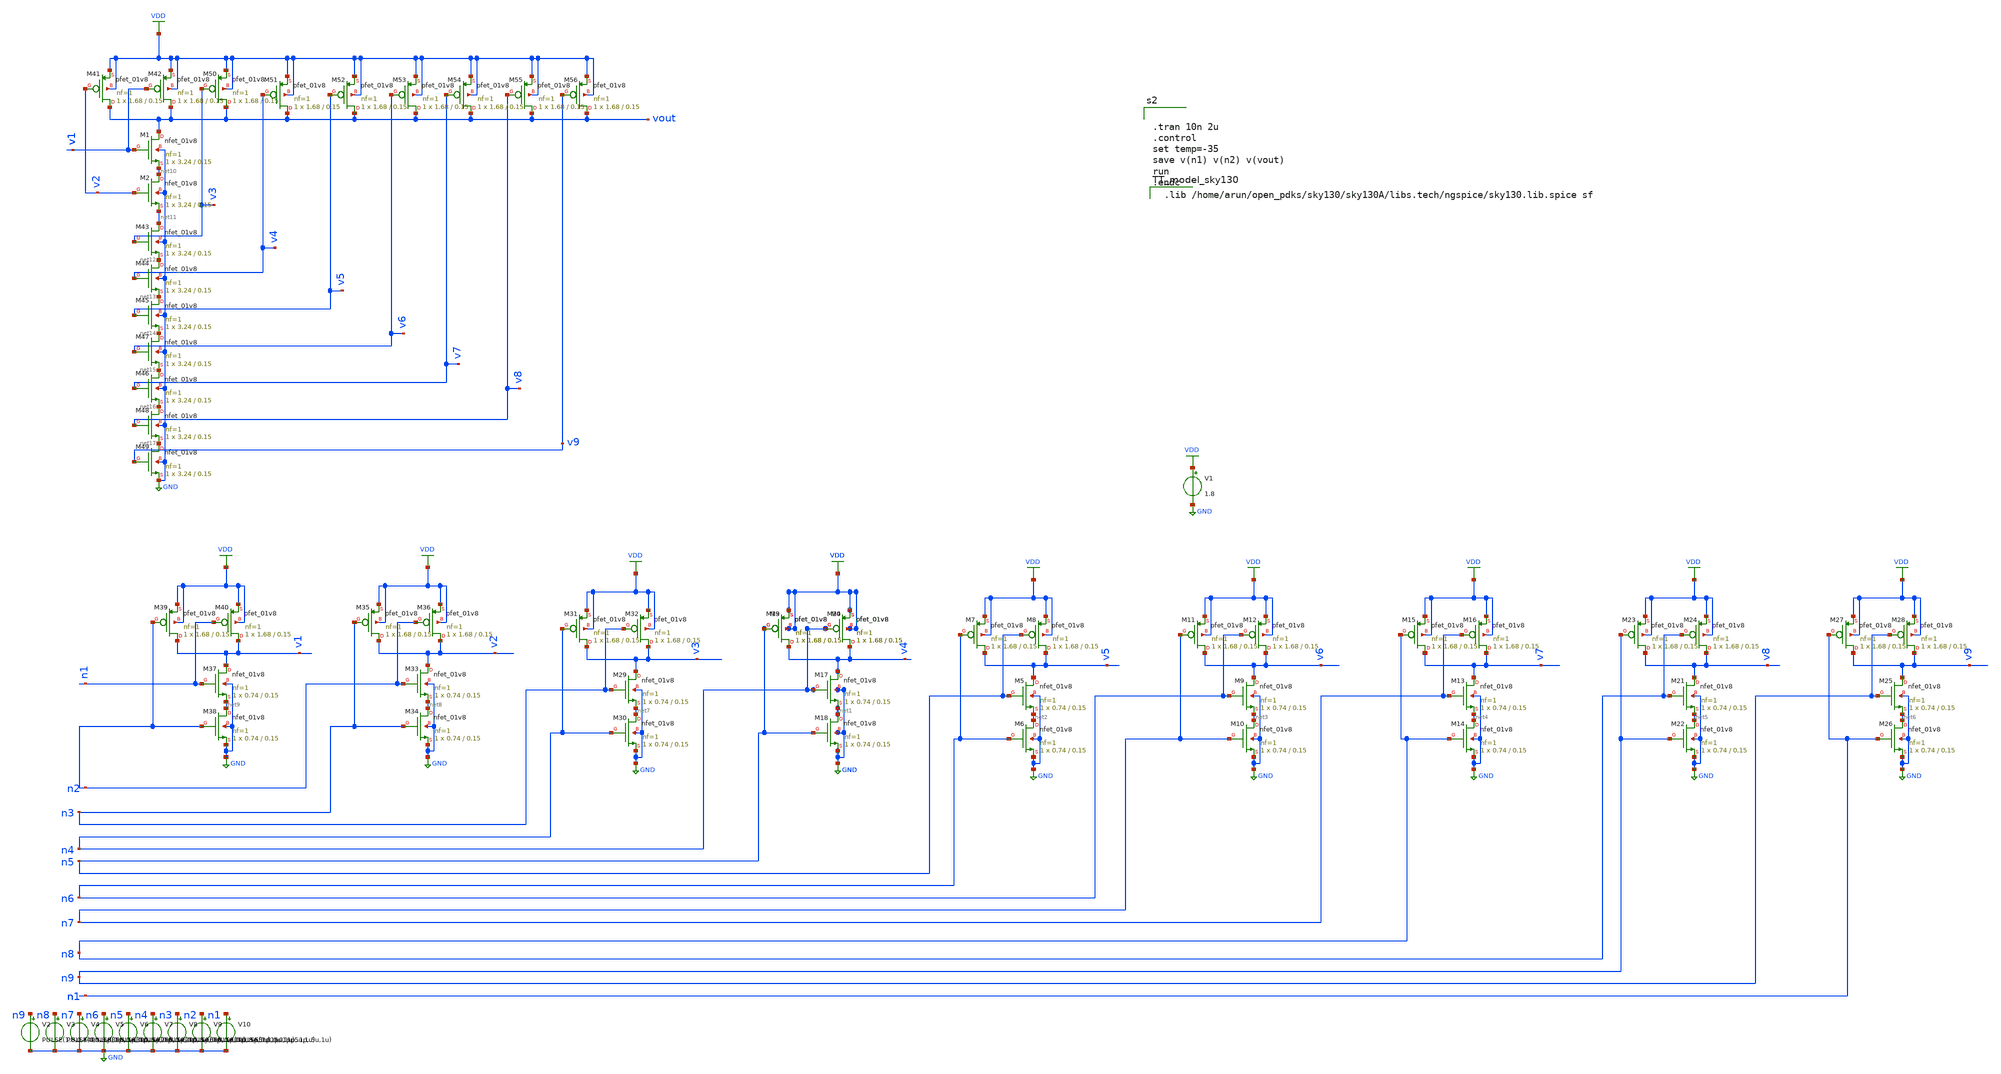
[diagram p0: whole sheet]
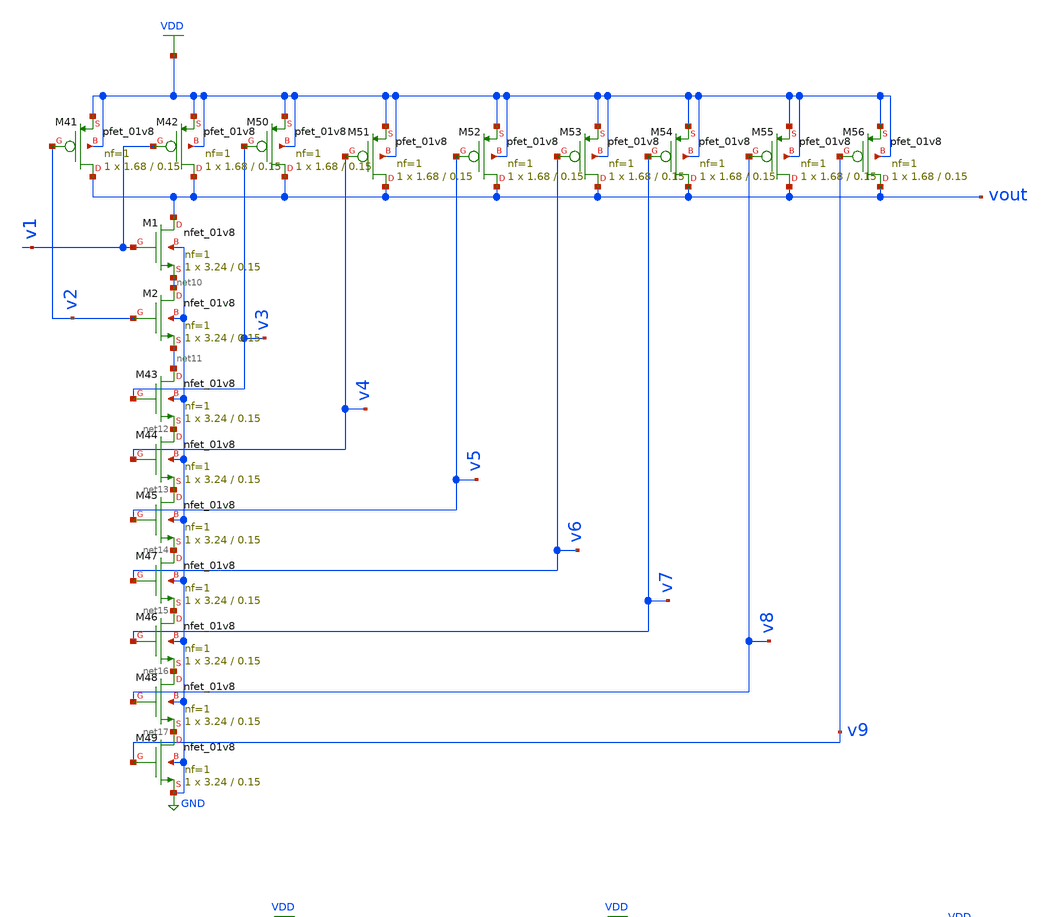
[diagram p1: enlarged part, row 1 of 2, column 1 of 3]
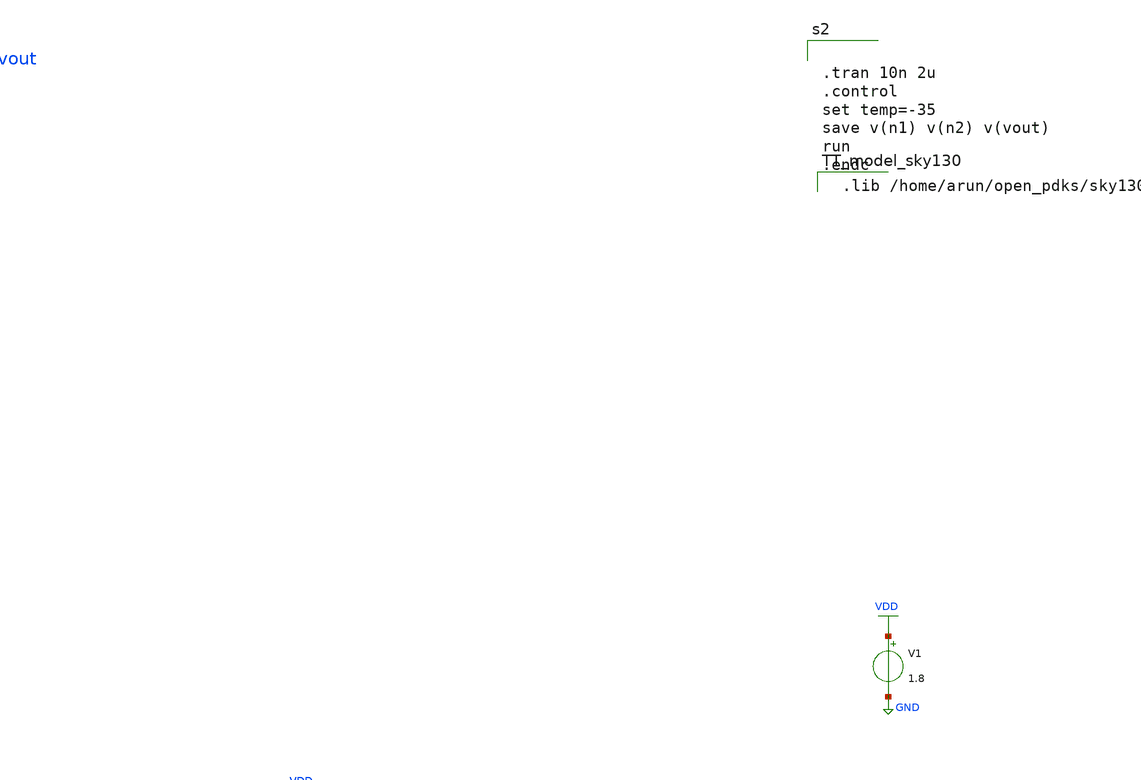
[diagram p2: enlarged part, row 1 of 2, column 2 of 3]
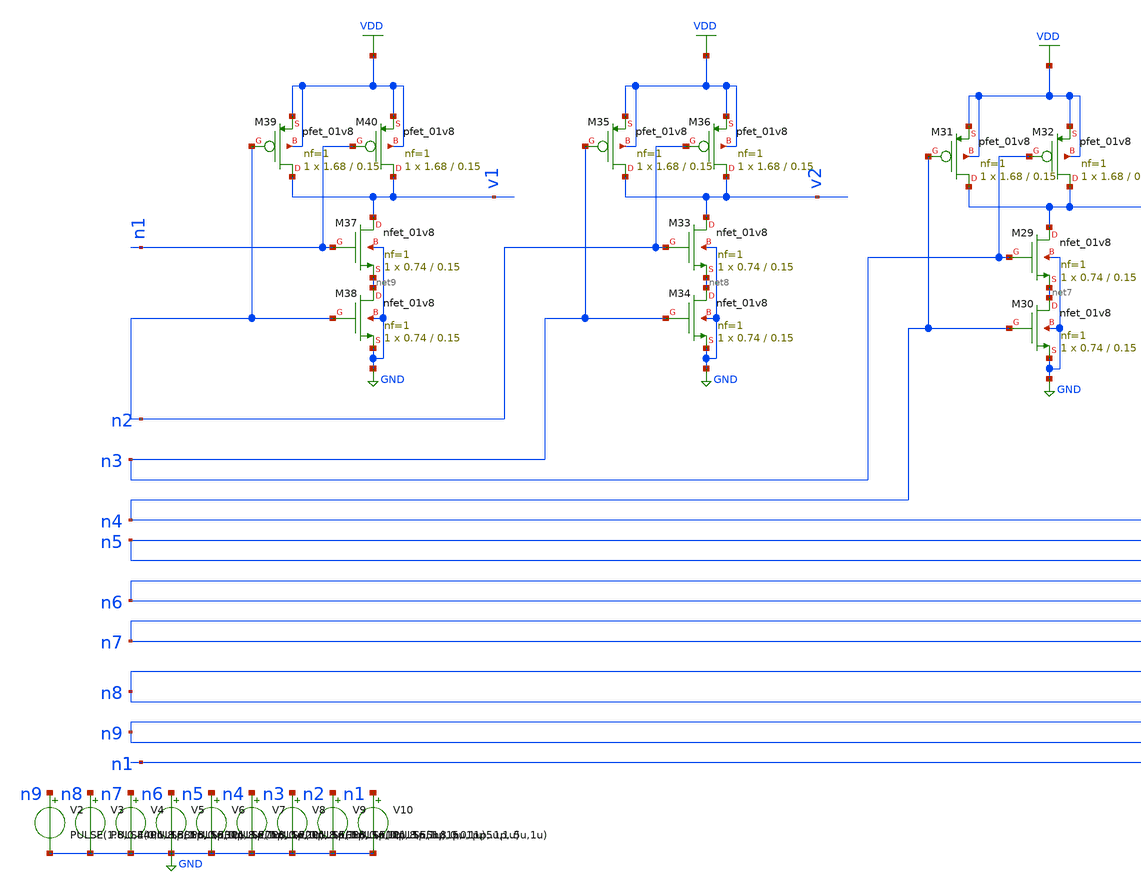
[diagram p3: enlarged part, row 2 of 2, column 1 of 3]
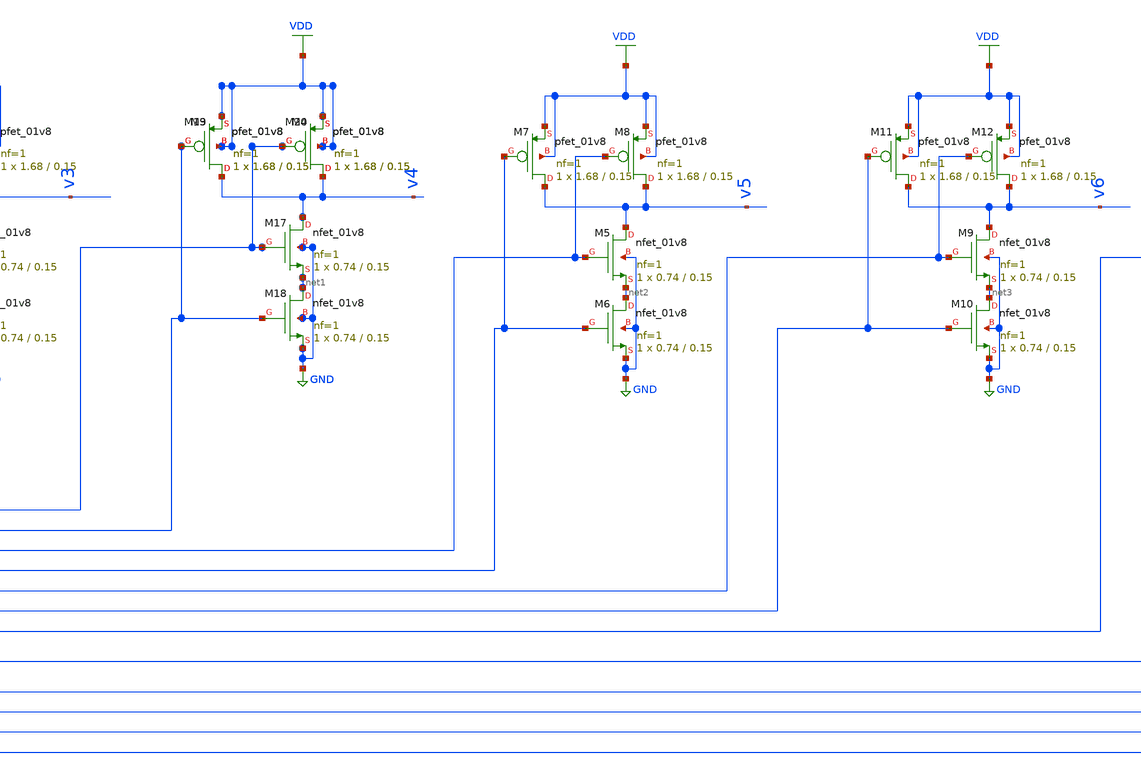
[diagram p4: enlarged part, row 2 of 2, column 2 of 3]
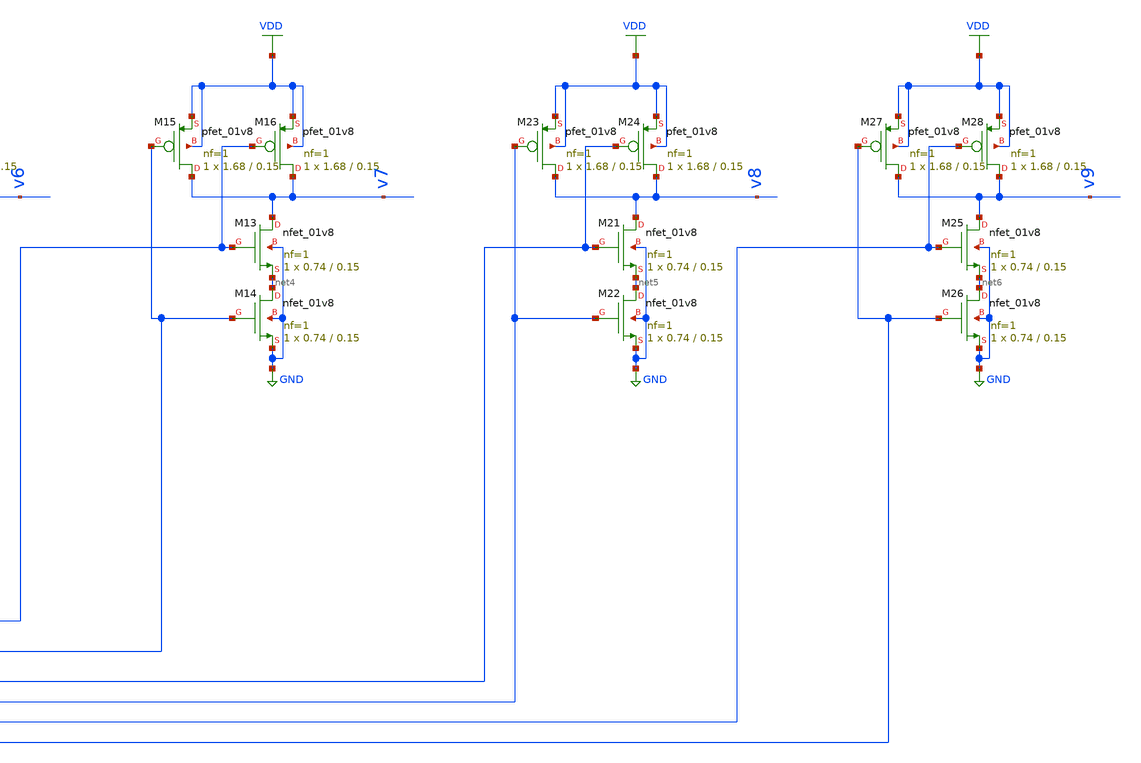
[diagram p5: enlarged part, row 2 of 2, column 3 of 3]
** sch_path: prelayout simulations/edge/edgecombiner.sch
**.subckt edgecombiner
XM3 v4 n5 VDD VDD sky130_fd_pr__pfet_01v8 L=0.15 W=1.68 nf=1 ad='int((nf+1)/2) * W/nf * 0.29' as='int((nf+2)/2) * W/nf * 0.29'
+ pd='2*int((nf+1)/2) * (W/nf + 0.29)' ps='2*int((nf+2)/2) * (W/nf + 0.29)' nrd='0.29 / W' nrs='0.29 / W'
+ sa=0 sb=0 sd=0 mult=1 m=1
XM4 v4 n4 VDD VDD sky130_fd_pr__pfet_01v8 L=0.15 W=1.68 nf=1 ad='int((nf+1)/2) * W/nf * 0.29' as='int((nf+2)/2) * W/nf * 0.29'
+ pd='2*int((nf+1)/2) * (W/nf + 0.29)' ps='2*int((nf+2)/2) * (W/nf + 0.29)' nrd='0.29 / W' nrs='0.29 / W'
+ sa=0 sb=0 sd=0 mult=1 m=1
XM5 v5 n5 net2 GND sky130_fd_pr__nfet_01v8 L=0.15 W=0.74 nf=1 ad='int((nf+1)/2) * W/nf * 0.29' as='int((nf+2)/2) * W/nf * 0.29'
+ pd='2*int((nf+1)/2) * (W/nf + 0.29)' ps='2*int((nf+2)/2) * (W/nf + 0.29)' nrd='0.29 / W' nrs='0.29 / W'
+ sa=0 sb=0 sd=0 mult=1 m=1
XM6 net2 n6 GND GND sky130_fd_pr__nfet_01v8 L=0.15 W=0.74 nf=1 ad='int((nf+1)/2) * W/nf * 0.29' as='int((nf+2)/2) * W/nf * 0.29'
+ pd='2*int((nf+1)/2) * (W/nf + 0.29)' ps='2*int((nf+2)/2) * (W/nf + 0.29)' nrd='0.29 / W' nrs='0.29 / W'
+ sa=0 sb=0 sd=0 mult=1 m=1
XM7 v5 n6 VDD VDD sky130_fd_pr__pfet_01v8 L=0.15 W=1.68 nf=1 ad='int((nf+1)/2) * W/nf * 0.29' as='int((nf+2)/2) * W/nf * 0.29'
+ pd='2*int((nf+1)/2) * (W/nf + 0.29)' ps='2*int((nf+2)/2) * (W/nf + 0.29)' nrd='0.29 / W' nrs='0.29 / W'
+ sa=0 sb=0 sd=0 mult=1 m=1
XM8 v5 n5 VDD VDD sky130_fd_pr__pfet_01v8 L=0.15 W=1.68 nf=1 ad='int((nf+1)/2) * W/nf * 0.29' as='int((nf+2)/2) * W/nf * 0.29'
+ pd='2*int((nf+1)/2) * (W/nf + 0.29)' ps='2*int((nf+2)/2) * (W/nf + 0.29)' nrd='0.29 / W' nrs='0.29 / W'
+ sa=0 sb=0 sd=0 mult=1 m=1
XM9 v6 n6 net3 GND sky130_fd_pr__nfet_01v8 L=0.15 W=0.74 nf=1 ad='int((nf+1)/2) * W/nf * 0.29' as='int((nf+2)/2) * W/nf * 0.29'
+ pd='2*int((nf+1)/2) * (W/nf + 0.29)' ps='2*int((nf+2)/2) * (W/nf + 0.29)' nrd='0.29 / W' nrs='0.29 / W'
+ sa=0 sb=0 sd=0 mult=1 m=1
XM10 net3 n7 GND GND sky130_fd_pr__nfet_01v8 L=0.15 W=0.74 nf=1 ad='int((nf+1)/2) * W/nf * 0.29' as='int((nf+2)/2) * W/nf * 0.29'
+ pd='2*int((nf+1)/2) * (W/nf + 0.29)' ps='2*int((nf+2)/2) * (W/nf + 0.29)' nrd='0.29 / W' nrs='0.29 / W'
+ sa=0 sb=0 sd=0 mult=1 m=1
XM11 v6 n7 VDD VDD sky130_fd_pr__pfet_01v8 L=0.15 W=1.68 nf=1 ad='int((nf+1)/2) * W/nf * 0.29' as='int((nf+2)/2) * W/nf * 0.29'
+ pd='2*int((nf+1)/2) * (W/nf + 0.29)' ps='2*int((nf+2)/2) * (W/nf + 0.29)' nrd='0.29 / W' nrs='0.29 / W'
+ sa=0 sb=0 sd=0 mult=1 m=1
XM12 v6 n6 VDD VDD sky130_fd_pr__pfet_01v8 L=0.15 W=1.68 nf=1 ad='int((nf+1)/2) * W/nf * 0.29' as='int((nf+2)/2) * W/nf * 0.29'
+ pd='2*int((nf+1)/2) * (W/nf + 0.29)' ps='2*int((nf+2)/2) * (W/nf + 0.29)' nrd='0.29 / W' nrs='0.29 / W'
+ sa=0 sb=0 sd=0 mult=1 m=1
XM13 v7 n7 net4 GND sky130_fd_pr__nfet_01v8 L=0.15 W=0.74 nf=1 ad='int((nf+1)/2) * W/nf * 0.29' as='int((nf+2)/2) * W/nf * 0.29'
+ pd='2*int((nf+1)/2) * (W/nf + 0.29)' ps='2*int((nf+2)/2) * (W/nf + 0.29)' nrd='0.29 / W' nrs='0.29 / W'
+ sa=0 sb=0 sd=0 mult=1 m=1
XM14 net4 n8 GND GND sky130_fd_pr__nfet_01v8 L=0.15 W=0.74 nf=1 ad='int((nf+1)/2) * W/nf * 0.29' as='int((nf+2)/2) * W/nf * 0.29'
+ pd='2*int((nf+1)/2) * (W/nf + 0.29)' ps='2*int((nf+2)/2) * (W/nf + 0.29)' nrd='0.29 / W' nrs='0.29 / W'
+ sa=0 sb=0 sd=0 mult=1 m=1
XM15 v7 n8 VDD VDD sky130_fd_pr__pfet_01v8 L=0.15 W=1.68 nf=1 ad='int((nf+1)/2) * W/nf * 0.29' as='int((nf+2)/2) * W/nf * 0.29'
+ pd='2*int((nf+1)/2) * (W/nf + 0.29)' ps='2*int((nf+2)/2) * (W/nf + 0.29)' nrd='0.29 / W' nrs='0.29 / W'
+ sa=0 sb=0 sd=0 mult=1 m=1
XM16 v7 n7 VDD VDD sky130_fd_pr__pfet_01v8 L=0.15 W=1.68 nf=1 ad='int((nf+1)/2) * W/nf * 0.29' as='int((nf+2)/2) * W/nf * 0.29'
+ pd='2*int((nf+1)/2) * (W/nf + 0.29)' ps='2*int((nf+2)/2) * (W/nf + 0.29)' nrd='0.29 / W' nrs='0.29 / W'
+ sa=0 sb=0 sd=0 mult=1 m=1
XM17 v4 n4 net1 GND sky130_fd_pr__nfet_01v8 L=0.15 W=0.74 nf=1 ad='int((nf+1)/2) * W/nf * 0.29' as='int((nf+2)/2) * W/nf * 0.29'
+ pd='2*int((nf+1)/2) * (W/nf + 0.29)' ps='2*int((nf+2)/2) * (W/nf + 0.29)' nrd='0.29 / W' nrs='0.29 / W'
+ sa=0 sb=0 sd=0 mult=1 m=1
XM18 net1 n5 GND GND sky130_fd_pr__nfet_01v8 L=0.15 W=0.74 nf=1 ad='int((nf+1)/2) * W/nf * 0.29' as='int((nf+2)/2) * W/nf * 0.29'
+ pd='2*int((nf+1)/2) * (W/nf + 0.29)' ps='2*int((nf+2)/2) * (W/nf + 0.29)' nrd='0.29 / W' nrs='0.29 / W'
+ sa=0 sb=0 sd=0 mult=1 m=1
XM19 v4 n5 VDD VDD sky130_fd_pr__pfet_01v8 L=0.15 W=1.68 nf=1 ad='int((nf+1)/2) * W/nf * 0.29' as='int((nf+2)/2) * W/nf * 0.29'
+ pd='2*int((nf+1)/2) * (W/nf + 0.29)' ps='2*int((nf+2)/2) * (W/nf + 0.29)' nrd='0.29 / W' nrs='0.29 / W'
+ sa=0 sb=0 sd=0 mult=1 m=1
XM20 v4 n4 VDD VDD sky130_fd_pr__pfet_01v8 L=0.15 W=1.68 nf=1 ad='int((nf+1)/2) * W/nf * 0.29' as='int((nf+2)/2) * W/nf * 0.29'
+ pd='2*int((nf+1)/2) * (W/nf + 0.29)' ps='2*int((nf+2)/2) * (W/nf + 0.29)' nrd='0.29 / W' nrs='0.29 / W'
+ sa=0 sb=0 sd=0 mult=1 m=1
XM21 v8 n8 net5 GND sky130_fd_pr__nfet_01v8 L=0.15 W=0.74 nf=1 ad='int((nf+1)/2) * W/nf * 0.29' as='int((nf+2)/2) * W/nf * 0.29'
+ pd='2*int((nf+1)/2) * (W/nf + 0.29)' ps='2*int((nf+2)/2) * (W/nf + 0.29)' nrd='0.29 / W' nrs='0.29 / W'
+ sa=0 sb=0 sd=0 mult=1 m=1
XM22 net5 n9 GND GND sky130_fd_pr__nfet_01v8 L=0.15 W=0.74 nf=1 ad='int((nf+1)/2) * W/nf * 0.29' as='int((nf+2)/2) * W/nf * 0.29'
+ pd='2*int((nf+1)/2) * (W/nf + 0.29)' ps='2*int((nf+2)/2) * (W/nf + 0.29)' nrd='0.29 / W' nrs='0.29 / W'
+ sa=0 sb=0 sd=0 mult=1 m=1
XM23 v8 n9 VDD VDD sky130_fd_pr__pfet_01v8 L=0.15 W=1.68 nf=1 ad='int((nf+1)/2) * W/nf * 0.29' as='int((nf+2)/2) * W/nf * 0.29'
+ pd='2*int((nf+1)/2) * (W/nf + 0.29)' ps='2*int((nf+2)/2) * (W/nf + 0.29)' nrd='0.29 / W' nrs='0.29 / W'
+ sa=0 sb=0 sd=0 mult=1 m=1
XM24 v8 n8 VDD VDD sky130_fd_pr__pfet_01v8 L=0.15 W=1.68 nf=1 ad='int((nf+1)/2) * W/nf * 0.29' as='int((nf+2)/2) * W/nf * 0.29'
+ pd='2*int((nf+1)/2) * (W/nf + 0.29)' ps='2*int((nf+2)/2) * (W/nf + 0.29)' nrd='0.29 / W' nrs='0.29 / W'
+ sa=0 sb=0 sd=0 mult=1 m=1
XM25 v9 n9 net6 GND sky130_fd_pr__nfet_01v8 L=0.15 W=0.74 nf=1 ad='int((nf+1)/2) * W/nf * 0.29' as='int((nf+2)/2) * W/nf * 0.29'
+ pd='2*int((nf+1)/2) * (W/nf + 0.29)' ps='2*int((nf+2)/2) * (W/nf + 0.29)' nrd='0.29 / W' nrs='0.29 / W'
+ sa=0 sb=0 sd=0 mult=1 m=1
XM26 net6 n1 GND GND sky130_fd_pr__nfet_01v8 L=0.15 W=0.74 nf=1 ad='int((nf+1)/2) * W/nf * 0.29' as='int((nf+2)/2) * W/nf * 0.29'
+ pd='2*int((nf+1)/2) * (W/nf + 0.29)' ps='2*int((nf+2)/2) * (W/nf + 0.29)' nrd='0.29 / W' nrs='0.29 / W'
+ sa=0 sb=0 sd=0 mult=1 m=1
XM27 v9 n1 VDD VDD sky130_fd_pr__pfet_01v8 L=0.15 W=1.68 nf=1 ad='int((nf+1)/2) * W/nf * 0.29' as='int((nf+2)/2) * W/nf * 0.29'
+ pd='2*int((nf+1)/2) * (W/nf + 0.29)' ps='2*int((nf+2)/2) * (W/nf + 0.29)' nrd='0.29 / W' nrs='0.29 / W'
+ sa=0 sb=0 sd=0 mult=1 m=1
XM28 v9 n9 VDD VDD sky130_fd_pr__pfet_01v8 L=0.15 W=1.68 nf=1 ad='int((nf+1)/2) * W/nf * 0.29' as='int((nf+2)/2) * W/nf * 0.29'
+ pd='2*int((nf+1)/2) * (W/nf + 0.29)' ps='2*int((nf+2)/2) * (W/nf + 0.29)' nrd='0.29 / W' nrs='0.29 / W'
+ sa=0 sb=0 sd=0 mult=1 m=1
XM29 v3 n3 net7 GND sky130_fd_pr__nfet_01v8 L=0.15 W=0.74 nf=1 ad='int((nf+1)/2) * W/nf * 0.29' as='int((nf+2)/2) * W/nf * 0.29'
+ pd='2*int((nf+1)/2) * (W/nf + 0.29)' ps='2*int((nf+2)/2) * (W/nf + 0.29)' nrd='0.29 / W' nrs='0.29 / W'
+ sa=0 sb=0 sd=0 mult=1 m=1
XM30 net7 n4 GND GND sky130_fd_pr__nfet_01v8 L=0.15 W=0.74 nf=1 ad='int((nf+1)/2) * W/nf * 0.29' as='int((nf+2)/2) * W/nf * 0.29'
+ pd='2*int((nf+1)/2) * (W/nf + 0.29)' ps='2*int((nf+2)/2) * (W/nf + 0.29)' nrd='0.29 / W' nrs='0.29 / W'
+ sa=0 sb=0 sd=0 mult=1 m=1
XM31 v3 n4 VDD VDD sky130_fd_pr__pfet_01v8 L=0.15 W=1.68 nf=1 ad='int((nf+1)/2) * W/nf * 0.29' as='int((nf+2)/2) * W/nf * 0.29'
+ pd='2*int((nf+1)/2) * (W/nf + 0.29)' ps='2*int((nf+2)/2) * (W/nf + 0.29)' nrd='0.29 / W' nrs='0.29 / W'
+ sa=0 sb=0 sd=0 mult=1 m=1
XM32 v3 n3 VDD VDD sky130_fd_pr__pfet_01v8 L=0.15 W=1.68 nf=1 ad='int((nf+1)/2) * W/nf * 0.29' as='int((nf+2)/2) * W/nf * 0.29'
+ pd='2*int((nf+1)/2) * (W/nf + 0.29)' ps='2*int((nf+2)/2) * (W/nf + 0.29)' nrd='0.29 / W' nrs='0.29 / W'
+ sa=0 sb=0 sd=0 mult=1 m=1
XM33 v2 n2 net8 GND sky130_fd_pr__nfet_01v8 L=0.15 W=0.74 nf=1 ad='int((nf+1)/2) * W/nf * 0.29' as='int((nf+2)/2) * W/nf * 0.29'
+ pd='2*int((nf+1)/2) * (W/nf + 0.29)' ps='2*int((nf+2)/2) * (W/nf + 0.29)' nrd='0.29 / W' nrs='0.29 / W'
+ sa=0 sb=0 sd=0 mult=1 m=1
XM34 net8 n3 GND GND sky130_fd_pr__nfet_01v8 L=0.15 W=0.74 nf=1 ad='int((nf+1)/2) * W/nf * 0.29' as='int((nf+2)/2) * W/nf * 0.29'
+ pd='2*int((nf+1)/2) * (W/nf + 0.29)' ps='2*int((nf+2)/2) * (W/nf + 0.29)' nrd='0.29 / W' nrs='0.29 / W'
+ sa=0 sb=0 sd=0 mult=1 m=1
XM35 v2 n3 VDD VDD sky130_fd_pr__pfet_01v8 L=0.15 W=1.68 nf=1 ad='int((nf+1)/2) * W/nf * 0.29' as='int((nf+2)/2) * W/nf * 0.29'
+ pd='2*int((nf+1)/2) * (W/nf + 0.29)' ps='2*int((nf+2)/2) * (W/nf + 0.29)' nrd='0.29 / W' nrs='0.29 / W'
+ sa=0 sb=0 sd=0 mult=1 m=1
XM36 v2 n2 VDD VDD sky130_fd_pr__pfet_01v8 L=0.15 W=1.68 nf=1 ad='int((nf+1)/2) * W/nf * 0.29' as='int((nf+2)/2) * W/nf * 0.29'
+ pd='2*int((nf+1)/2) * (W/nf + 0.29)' ps='2*int((nf+2)/2) * (W/nf + 0.29)' nrd='0.29 / W' nrs='0.29 / W'
+ sa=0 sb=0 sd=0 mult=1 m=1
XM37 v1 n1 net9 GND sky130_fd_pr__nfet_01v8 L=0.15 W=0.74 nf=1 ad='int((nf+1)/2) * W/nf * 0.29' as='int((nf+2)/2) * W/nf * 0.29'
+ pd='2*int((nf+1)/2) * (W/nf + 0.29)' ps='2*int((nf+2)/2) * (W/nf + 0.29)' nrd='0.29 / W' nrs='0.29 / W'
+ sa=0 sb=0 sd=0 mult=1 m=1
XM38 net9 n2 GND GND sky130_fd_pr__nfet_01v8 L=0.15 W=0.74 nf=1 ad='int((nf+1)/2) * W/nf * 0.29' as='int((nf+2)/2) * W/nf * 0.29'
+ pd='2*int((nf+1)/2) * (W/nf + 0.29)' ps='2*int((nf+2)/2) * (W/nf + 0.29)' nrd='0.29 / W' nrs='0.29 / W'
+ sa=0 sb=0 sd=0 mult=1 m=1
XM39 v1 n2 VDD VDD sky130_fd_pr__pfet_01v8 L=0.15 W=1.68 nf=1 ad='int((nf+1)/2) * W/nf * 0.29' as='int((nf+2)/2) * W/nf * 0.29'
+ pd='2*int((nf+1)/2) * (W/nf + 0.29)' ps='2*int((nf+2)/2) * (W/nf + 0.29)' nrd='0.29 / W' nrs='0.29 / W'
+ sa=0 sb=0 sd=0 mult=1 m=1
XM40 v1 n1 VDD VDD sky130_fd_pr__pfet_01v8 L=0.15 W=1.68 nf=1 ad='int((nf+1)/2) * W/nf * 0.29' as='int((nf+2)/2) * W/nf * 0.29'
+ pd='2*int((nf+1)/2) * (W/nf + 0.29)' ps='2*int((nf+2)/2) * (W/nf + 0.29)' nrd='0.29 / W' nrs='0.29 / W'
+ sa=0 sb=0 sd=0 mult=1 m=1
V1 VDD GND 1.8
XM1 vout v1 net10 GND sky130_fd_pr__nfet_01v8 L=0.15 W=3.24 nf=1 ad='int((nf+1)/2) * W/nf * 0.29' as='int((nf+2)/2) * W/nf * 0.29'
+ pd='2*int((nf+1)/2) * (W/nf + 0.29)' ps='2*int((nf+2)/2) * (W/nf + 0.29)' nrd='0.29 / W' nrs='0.29 / W'
+ sa=0 sb=0 sd=0 mult=1 m=1
XM2 net10 v2 net11 GND sky130_fd_pr__nfet_01v8 L=0.15 W=3.24 nf=1 ad='int((nf+1)/2) * W/nf * 0.29' as='int((nf+2)/2) * W/nf * 0.29'
+ pd='2*int((nf+1)/2) * (W/nf + 0.29)' ps='2*int((nf+2)/2) * (W/nf + 0.29)' nrd='0.29 / W' nrs='0.29 / W'
+ sa=0 sb=0 sd=0 mult=1 m=1
XM41 vout v2 VDD VDD sky130_fd_pr__pfet_01v8 L=0.15 W=1.68 nf=1 ad='int((nf+1)/2) * W/nf * 0.29' as='int((nf+2)/2) * W/nf * 0.29'
+ pd='2*int((nf+1)/2) * (W/nf + 0.29)' ps='2*int((nf+2)/2) * (W/nf + 0.29)' nrd='0.29 / W' nrs='0.29 / W'
+ sa=0 sb=0 sd=0 mult=1 m=1
XM42 vout v1 VDD VDD sky130_fd_pr__pfet_01v8 L=0.15 W=1.68 nf=1 ad='int((nf+1)/2) * W/nf * 0.29' as='int((nf+2)/2) * W/nf * 0.29'
+ pd='2*int((nf+1)/2) * (W/nf + 0.29)' ps='2*int((nf+2)/2) * (W/nf + 0.29)' nrd='0.29 / W' nrs='0.29 / W'
+ sa=0 sb=0 sd=0 mult=1 m=1
XM43 net11 v3 net12 GND sky130_fd_pr__nfet_01v8 L=0.15 W=3.24 nf=1 ad='int((nf+1)/2) * W/nf * 0.29' as='int((nf+2)/2) * W/nf * 0.29'
+ pd='2*int((nf+1)/2) * (W/nf + 0.29)' ps='2*int((nf+2)/2) * (W/nf + 0.29)' nrd='0.29 / W' nrs='0.29 / W'
+ sa=0 sb=0 sd=0 mult=1 m=1
XM44 net12 v4 net13 GND sky130_fd_pr__nfet_01v8 L=0.15 W=3.24 nf=1 ad='int((nf+1)/2) * W/nf * 0.29' as='int((nf+2)/2) * W/nf * 0.29'
+ pd='2*int((nf+1)/2) * (W/nf + 0.29)' ps='2*int((nf+2)/2) * (W/nf + 0.29)' nrd='0.29 / W' nrs='0.29 / W'
+ sa=0 sb=0 sd=0 mult=1 m=1
XM45 net13 v5 net14 GND sky130_fd_pr__nfet_01v8 L=0.15 W=3.24 nf=1 ad='int((nf+1)/2) * W/nf * 0.29' as='int((nf+2)/2) * W/nf * 0.29'
+ pd='2*int((nf+1)/2) * (W/nf + 0.29)' ps='2*int((nf+2)/2) * (W/nf + 0.29)' nrd='0.29 / W' nrs='0.29 / W'
+ sa=0 sb=0 sd=0 mult=1 m=1
XM46 net15 v7 net16 GND sky130_fd_pr__nfet_01v8 L=0.15 W=3.24 nf=1 ad='int((nf+1)/2) * W/nf * 0.29' as='int((nf+2)/2) * W/nf * 0.29'
+ pd='2*int((nf+1)/2) * (W/nf + 0.29)' ps='2*int((nf+2)/2) * (W/nf + 0.29)' nrd='0.29 / W' nrs='0.29 / W'
+ sa=0 sb=0 sd=0 mult=1 m=1
XM47 net14 v6 net15 GND sky130_fd_pr__nfet_01v8 L=0.15 W=3.24 nf=1 ad='int((nf+1)/2) * W/nf * 0.29' as='int((nf+2)/2) * W/nf * 0.29'
+ pd='2*int((nf+1)/2) * (W/nf + 0.29)' ps='2*int((nf+2)/2) * (W/nf + 0.29)' nrd='0.29 / W' nrs='0.29 / W'
+ sa=0 sb=0 sd=0 mult=1 m=1
XM48 net16 v8 net17 GND sky130_fd_pr__nfet_01v8 L=0.15 W=3.24 nf=1 ad='int((nf+1)/2) * W/nf * 0.29' as='int((nf+2)/2) * W/nf * 0.29'
+ pd='2*int((nf+1)/2) * (W/nf + 0.29)' ps='2*int((nf+2)/2) * (W/nf + 0.29)' nrd='0.29 / W' nrs='0.29 / W'
+ sa=0 sb=0 sd=0 mult=1 m=1
XM49 net17 v9 GND GND sky130_fd_pr__nfet_01v8 L=0.15 W=3.24 nf=1 ad='int((nf+1)/2) * W/nf * 0.29' as='int((nf+2)/2) * W/nf * 0.29'
+ pd='2*int((nf+1)/2) * (W/nf + 0.29)' ps='2*int((nf+2)/2) * (W/nf + 0.29)' nrd='0.29 / W' nrs='0.29 / W'
+ sa=0 sb=0 sd=0 mult=1 m=1
XM51 vout v4 VDD VDD sky130_fd_pr__pfet_01v8 L=0.15 W=1.68 nf=1 ad='int((nf+1)/2) * W/nf * 0.29' as='int((nf+2)/2) * W/nf * 0.29'
+ pd='2*int((nf+1)/2) * (W/nf + 0.29)' ps='2*int((nf+2)/2) * (W/nf + 0.29)' nrd='0.29 / W' nrs='0.29 / W'
+ sa=0 sb=0 sd=0 mult=1 m=1
XM52 vout v5 VDD VDD sky130_fd_pr__pfet_01v8 L=0.15 W=1.68 nf=1 ad='int((nf+1)/2) * W/nf * 0.29' as='int((nf+2)/2) * W/nf * 0.29'
+ pd='2*int((nf+1)/2) * (W/nf + 0.29)' ps='2*int((nf+2)/2) * (W/nf + 0.29)' nrd='0.29 / W' nrs='0.29 / W'
+ sa=0 sb=0 sd=0 mult=1 m=1
XM53 vout v6 VDD VDD sky130_fd_pr__pfet_01v8 L=0.15 W=1.68 nf=1 ad='int((nf+1)/2) * W/nf * 0.29' as='int((nf+2)/2) * W/nf * 0.29'
+ pd='2*int((nf+1)/2) * (W/nf + 0.29)' ps='2*int((nf+2)/2) * (W/nf + 0.29)' nrd='0.29 / W' nrs='0.29 / W'
+ sa=0 sb=0 sd=0 mult=1 m=1
XM54 vout v7 VDD VDD sky130_fd_pr__pfet_01v8 L=0.15 W=1.68 nf=1 ad='int((nf+1)/2) * W/nf * 0.29' as='int((nf+2)/2) * W/nf * 0.29'
+ pd='2*int((nf+1)/2) * (W/nf + 0.29)' ps='2*int((nf+2)/2) * (W/nf + 0.29)' nrd='0.29 / W' nrs='0.29 / W'
+ sa=0 sb=0 sd=0 mult=1 m=1
XM55 vout v8 VDD VDD sky130_fd_pr__pfet_01v8 L=0.15 W=1.68 nf=1 ad='int((nf+1)/2) * W/nf * 0.29' as='int((nf+2)/2) * W/nf * 0.29'
+ pd='2*int((nf+1)/2) * (W/nf + 0.29)' ps='2*int((nf+2)/2) * (W/nf + 0.29)' nrd='0.29 / W' nrs='0.29 / W'
+ sa=0 sb=0 sd=0 mult=1 m=1
XM56 vout v9 VDD VDD sky130_fd_pr__pfet_01v8 L=0.15 W=1.68 nf=1 ad='int((nf+1)/2) * W/nf * 0.29' as='int((nf+2)/2) * W/nf * 0.29'
+ pd='2*int((nf+1)/2) * (W/nf + 0.29)' ps='2*int((nf+2)/2) * (W/nf + 0.29)' nrd='0.29 / W' nrs='0.29 / W'
+ sa=0 sb=0 sd=0 mult=1 m=1
XM50 vout v3 VDD VDD sky130_fd_pr__pfet_01v8 L=0.15 W=1.68 nf=1 ad='int((nf+1)/2) * W/nf * 0.29' as='int((nf+2)/2) * W/nf * 0.29'
+ pd='2*int((nf+1)/2) * (W/nf + 0.29)' ps='2*int((nf+2)/2) * (W/nf + 0.29)' nrd='0.29 / W' nrs='0.29 / W'
+ sa=0 sb=0 sd=0 mult=1 m=1
V2 n9 GND PULSE(1.8,0,440n,.1p,.1p,.5u,1u)
V3 n8 GND PULSE(0,1.8,385n,.1p,.1p,.5u,1u)
V4 n7 GND PULSE(1.8,0,330n,.1p,.1p,.5u,1u)
V5 n6 GND PULSE(0,1.8,275n,.1p,.1p,.5u,1u)
V6 n5 GND PULSE(1.8,0,220n,.1p,.1p,.5u,1u)
V7 n4 GND PULSE(0,1.8,165n,.1p,.1p,.5u,1u)
V8 n3 GND PULSE(1.8,0,110n,.1p,.1p,.5u,1u)
V9 n2 GND PULSE(0,1.8,55n,.1p,.1p,.5u,1u)
V10 n1 GND PULSE(1.8,0,0,.1p,.1p,.5u,1u)
**** begin user architecture code
 .lib /home/arun/open_pdks/sky130/sky130A/libs.tech/ngspice/sky130.lib.spice sf


.tran 10n 2u
.control
set temp=-35
save v(n1) v(n2) v(vout)
run
.endc

**** end user architecture code
**.ends
.GLOBAL VDD
.GLOBAL GND
.end
